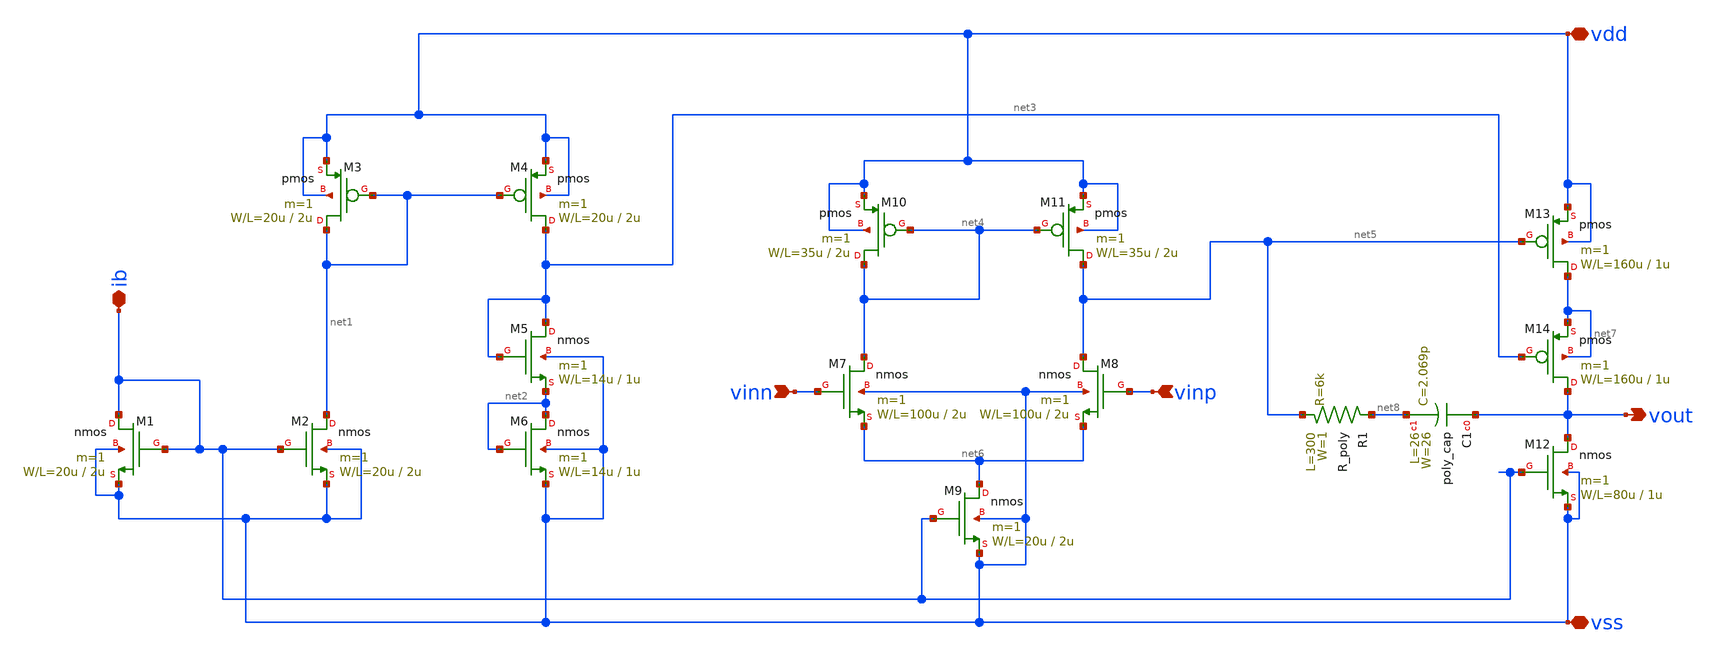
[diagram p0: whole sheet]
** sch_path: member_project/GroupWork/Team_masahiro/opamp.sch
**.subckt opamp vinn vinp vss vdd vout ib
*.ipin vinn
*.ipin vinp
*.iopin vss
*.iopin vdd
*.opin vout
*.iopin ib
M1 ib ib vss vss nmos L=2u W=20u m=1
M2 net1 ib vss vss nmos L=2u W=20u m=1
M3 net1 net1 vdd vdd pmos L=2u W=20u m=1
M4 net3 net1 vdd vdd pmos L=2u W=20u m=1
M5 net3 net3 net2 vss nmos L=1u W=14u m=1
M6 net2 net2 vss vss nmos L=1u W=14u m=1
M7 net4 vinn net6 vss nmos L=2u W=100u m=1
M8 net5 vinp net6 vss nmos L=2u W=100u m=1
M9 net6 ib vss vss nmos L=2u W=20u m=1
M10 net4 net4 vdd vdd pmos L=2u W=35u m=1
M11 net5 net4 vdd vdd pmos L=2u W=35u m=1
M12 vout ib vss vss nmos L=1u W=80u m=1
M13 net7 net5 vdd vdd pmos L=1u W=160u m=1
M14 vout net3 net7 net7 pmos L=1u W=160u m=1
C1 vout net8 poly_cap W=26 L=26
R1 net5 net8 R_poly W=1 L=300
**.ends
.end
